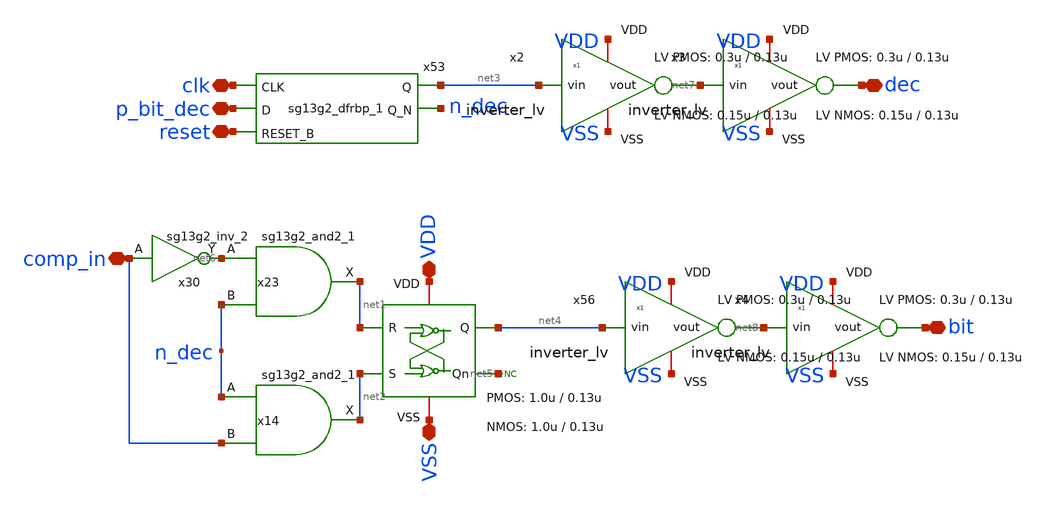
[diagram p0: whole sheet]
** sch_path: xschem/logic/bit_cell.sch
**.subckt bit_cell p_bit_dec clk reset comp_in VDD VSS bit dec
*.iopin p_bit_dec
*.iopin clk
*.iopin reset
*.iopin comp_in
*.iopin VDD
*.iopin VSS
*.iopin bit
*.iopin dec
x1 VDD net2 net5 VSS net4 net1 SR_latch W_P_SR=1.0u L_P_SR=0.13u W_N_SR=1.0u L_N_SR=0.13u
x23 net1 net6 n_dec VDD VSS sg13g2_and2_1
x14 net2 n_dec comp_in VDD VSS sg13g2_and2_1
x30 net6 comp_in VDD VSS sg13g2_inv_2
x53 net3 n_dec clk p_bit_dec reset VDD VSS sg13g2_dfrbp_1
* noconn #net5
x2 VDD net3 net7 VSS inverter_lv W_P=0.3u L_P=0.13u W_N=0.15u L_N=0.13u N_C=1
x56 VDD net4 net8 VSS inverter_lv W_P=0.3u L_P=0.13u W_N=0.15u L_N=0.13u N_C=1
x3 VDD net7 dec VSS inverter_lv W_P=0.3u L_P=0.13u W_N=0.15u L_N=0.13u N_C=1
x4 VDD net8 bit VSS inverter_lv W_P=0.3u L_P=0.13u W_N=0.15u L_N=0.13u N_C=1
**.ends
.end
